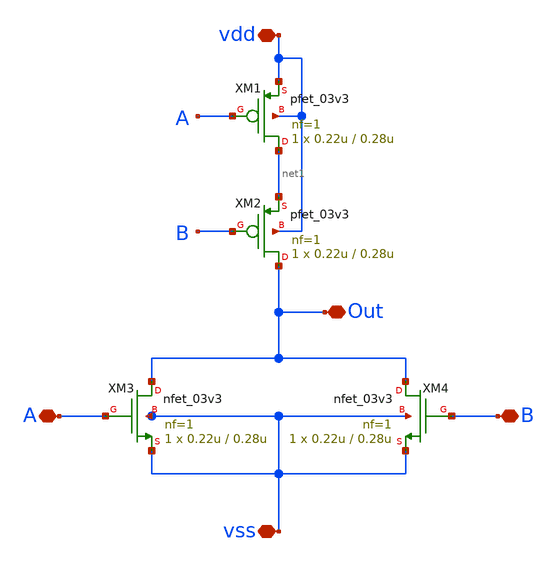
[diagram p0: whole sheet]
** sch_path: designs/libs/SIPO/or2.sch
**.subckt or2 vdd A B vss Out
*.iopin vdd
*.iopin A
*.iopin B
*.iopin vss
*.iopin Out
XM1 net1 A vdd vdd pfet_03v3 L=0.28u W=0.22u nf=1 ad='int((nf+1)/2) * W/nf * 0.18u' as='int((nf+2)/2) * W/nf * 0.18u'
+ pd='2*int((nf+1)/2) * (W/nf + 0.18u)' ps='2*int((nf+2)/2) * (W/nf + 0.18u)' nrd='0.18u / W' nrs='0.18u / W'
+ sa=0 sb=0 sd=0 m=1
XM2 Out B net1 vdd pfet_03v3 L=0.28u W=0.22u nf=1 ad='int((nf+1)/2) * W/nf * 0.18u' as='int((nf+2)/2) * W/nf * 0.18u'
+ pd='2*int((nf+1)/2) * (W/nf + 0.18u)' ps='2*int((nf+2)/2) * (W/nf + 0.18u)' nrd='0.18u / W' nrs='0.18u / W'
+ sa=0 sb=0 sd=0 m=1
XM3 Out A vss vss nfet_03v3 L=0.28u W=0.22u nf=1 ad='int((nf+1)/2) * W/nf * 0.18u' as='int((nf+2)/2) * W/nf * 0.18u'
+ pd='2*int((nf+1)/2) * (W/nf + 0.18u)' ps='2*int((nf+2)/2) * (W/nf + 0.18u)' nrd='0.18u / W' nrs='0.18u / W'
+ sa=0 sb=0 sd=0 m=1
XM4 Out B vss vss nfet_03v3 L=0.28u W=0.22u nf=1 ad='int((nf+1)/2) * W/nf * 0.18u' as='int((nf+2)/2) * W/nf * 0.18u'
+ pd='2*int((nf+1)/2) * (W/nf + 0.18u)' ps='2*int((nf+2)/2) * (W/nf + 0.18u)' nrd='0.18u / W' nrs='0.18u / W'
+ sa=0 sb=0 sd=0 m=1
**.ends
.end
